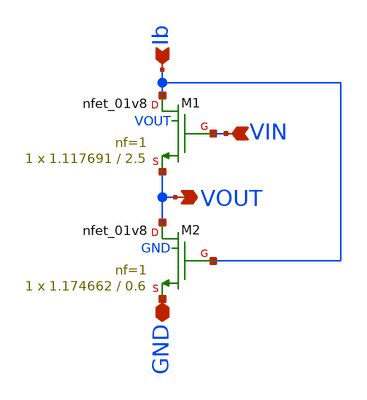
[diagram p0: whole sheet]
** sch_path: xschem/fvf.sch
**.subckt fvf VIN VOUT GND Ib
*.ipin VIN
*.opin VOUT
*.iopin GND
*.ipin Ib
XM1 Ib VIN VOUT VOUT sky130_fd_pr__nfet_01v8 L=2.5 W=1.117691 nf=1 ad='int((nf+1)/2) * W/nf * 0.29' as='int((nf+2)/2) * W/nf * 0.29'
+ pd='2*int((nf+1)/2) * (W/nf + 0.29)' ps='2*int((nf+2)/2) * (W/nf + 0.29)' nrd='0.29 / W' nrs='0.29 / W'
+ sa=0 sb=0 sd=0 mult=1 m=1
XM2 VOUT Ib GND GND sky130_fd_pr__nfet_01v8 L=0.6 W=1.174662 nf=1 ad='int((nf+1)/2) * W/nf * 0.29' as='int((nf+2)/2) * W/nf * 0.29'
+ pd='2*int((nf+1)/2) * (W/nf + 0.29)' ps='2*int((nf+2)/2) * (W/nf + 0.29)' nrd='0.29 / W' nrs='0.29 / W'
+ sa=0 sb=0 sd=0 mult=1 m=1
**.ends
.end
